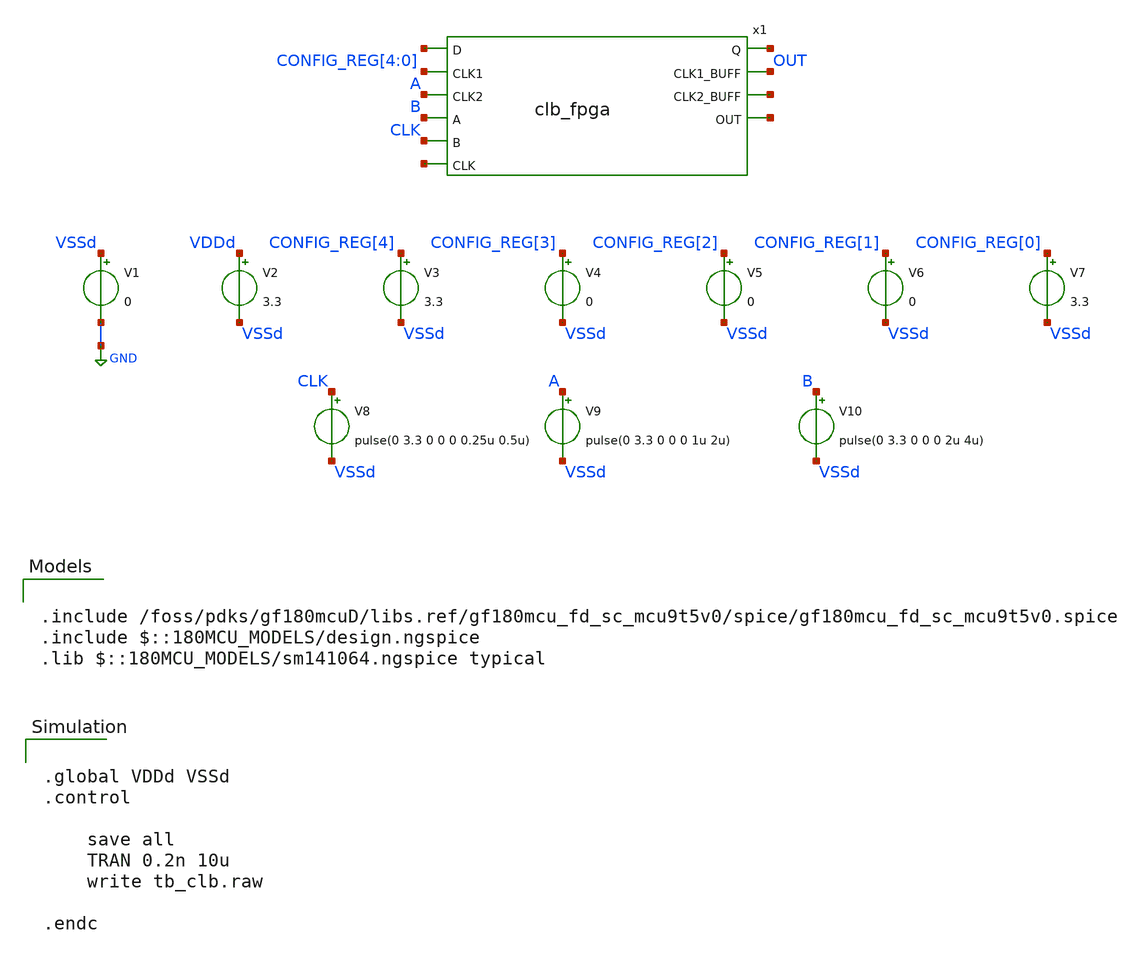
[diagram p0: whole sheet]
** sch_path: designs/libs/tb_fpga/tb_clb/tb_clb.sch
**.subckt tb_clb
x1 net1 CONFIG_REG[4] A B CLK net2 net3 OUT net4 net5 clb_fpga
V1 VSSd GND 0
V2 VDDd VSSd 3.3
V3 CONFIG_REG[4] VSSd 3.3
V4 CONFIG_REG[3] VSSd 0
V5 CONFIG_REG[2] VSSd 0
V6 CONFIG_REG[1] VSSd 0
V7 CONFIG_REG[0] VSSd 3.3
V8 CLK VSSd pulse(0 3.3 0 0 0 0.25u 0.5u)
V9 A VSSd pulse(0 3.3 0 0 0 1u 2u)
V10 B VSSd pulse(0 3.3 0 0 0 2u 4u)
**** begin user architecture code


.global VDDd VSSd
.control

    save all
    TRAN 0.2n 10u
    write tb_clb.raw

.endc



.include /foss/pdks/gf180mcuD/libs.ref/gf180mcu_fd_sc_mcu9t5v0/spice/gf180mcu_fd_sc_mcu9t5v0.spice
.include $::180MCU_MODELS/design.ngspice
.lib $::180MCU_MODELS/sm141064.ngspice typical

**** end user architecture code
**.ends
.GLOBAL GND
.end
